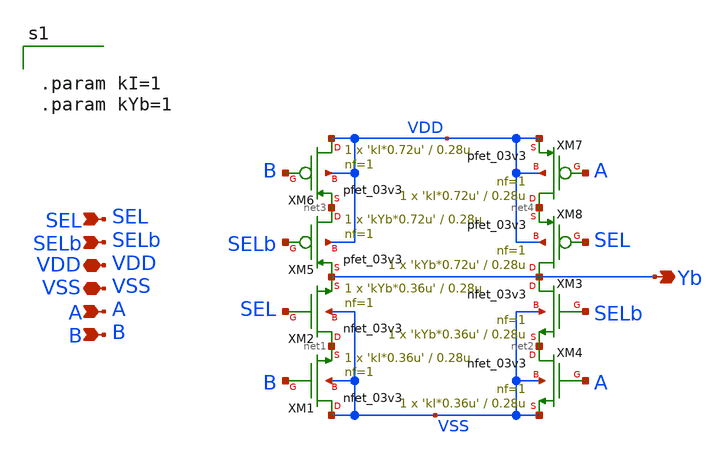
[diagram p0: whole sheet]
** sch_path: CAD5/2x1_muxb.sch
**.subckt 2x1_muxb A B SEL VDD VSS SELb Yb
*.ipin A
*.ipin B
*.ipin SEL
*.iopin VDD
*.iopin VSS
*.ipin SELb
*.opin Yb
XM1 VSS B net1 VSS nfet_03v3 L=0.28u W='kI*0.36u' nf=1 ad='int((nf+1)/2) * W/nf * 0.18u' as='int((nf+2)/2) * W/nf * 0.18u'
+ pd='2*int((nf+1)/2) * (W/nf + 0.18u)' ps='2*int((nf+2)/2) * (W/nf + 0.18u)' nrd='0.18u / W' nrs='0.18u / W'
+ sa=0 sb=0 sd=0 m=1
XM2 net1 SEL Yb VSS nfet_03v3 L=0.28u W='kYb*0.36u' nf=1 ad='int((nf+1)/2) * W/nf * 0.18u' as='int((nf+2)/2) * W/nf * 0.18u'
+ pd='2*int((nf+1)/2) * (W/nf + 0.18u)' ps='2*int((nf+2)/2) * (W/nf + 0.18u)' nrd='0.18u / W' nrs='0.18u / W'
+ sa=0 sb=0 sd=0 m=1
XM3 Yb SELb net2 VSS nfet_03v3 L=0.28u W='kYb*0.36u' nf=1 ad='int((nf+1)/2) * W/nf * 0.18u' as='int((nf+2)/2) * W/nf * 0.18u'
+ pd='2*int((nf+1)/2) * (W/nf + 0.18u)' ps='2*int((nf+2)/2) * (W/nf + 0.18u)' nrd='0.18u / W' nrs='0.18u / W'
+ sa=0 sb=0 sd=0 m=1
XM4 net2 A VSS VSS nfet_03v3 L=0.28u W='kI*0.36u' nf=1 ad='int((nf+1)/2) * W/nf * 0.18u' as='int((nf+2)/2) * W/nf * 0.18u'
+ pd='2*int((nf+1)/2) * (W/nf + 0.18u)' ps='2*int((nf+2)/2) * (W/nf + 0.18u)' nrd='0.18u / W' nrs='0.18u / W'
+ sa=0 sb=0 sd=0 m=1
XM5 net3 SELb Yb VDD pfet_03v3 L=0.28u W='kYb*0.72u' nf=1 ad='int((nf+1)/2) * W/nf * 0.18u' as='int((nf+2)/2) * W/nf * 0.18u'
+ pd='2*int((nf+1)/2) * (W/nf + 0.18u)' ps='2*int((nf+2)/2) * (W/nf + 0.18u)' nrd='0.18u / W' nrs='0.18u / W'
+ sa=0 sb=0 sd=0 m=1
XM6 VDD B net3 VDD pfet_03v3 L=0.28u W='kI*0.72u' nf=1 ad='int((nf+1)/2) * W/nf * 0.18u' as='int((nf+2)/2) * W/nf * 0.18u'
+ pd='2*int((nf+1)/2) * (W/nf + 0.18u)' ps='2*int((nf+2)/2) * (W/nf + 0.18u)' nrd='0.18u / W' nrs='0.18u / W'
+ sa=0 sb=0 sd=0 m=1
XM7 net4 A VDD VDD pfet_03v3 L=0.28u W='kI*0.72u' nf=1 ad='int((nf+1)/2) * W/nf * 0.18u' as='int((nf+2)/2) * W/nf * 0.18u'
+ pd='2*int((nf+1)/2) * (W/nf + 0.18u)' ps='2*int((nf+2)/2) * (W/nf + 0.18u)' nrd='0.18u / W' nrs='0.18u / W'
+ sa=0 sb=0 sd=0 m=1
XM8 Yb SEL net4 VDD pfet_03v3 L=0.28u W='kYb*0.72u' nf=1 ad='int((nf+1)/2) * W/nf * 0.18u' as='int((nf+2)/2) * W/nf * 0.18u'
+ pd='2*int((nf+1)/2) * (W/nf + 0.18u)' ps='2*int((nf+2)/2) * (W/nf + 0.18u)' nrd='0.18u / W' nrs='0.18u / W'
+ sa=0 sb=0 sd=0 m=1
**** begin user architecture code


.param kI=1
.param kYb=1


**** end user architecture code
**.ends
.end
